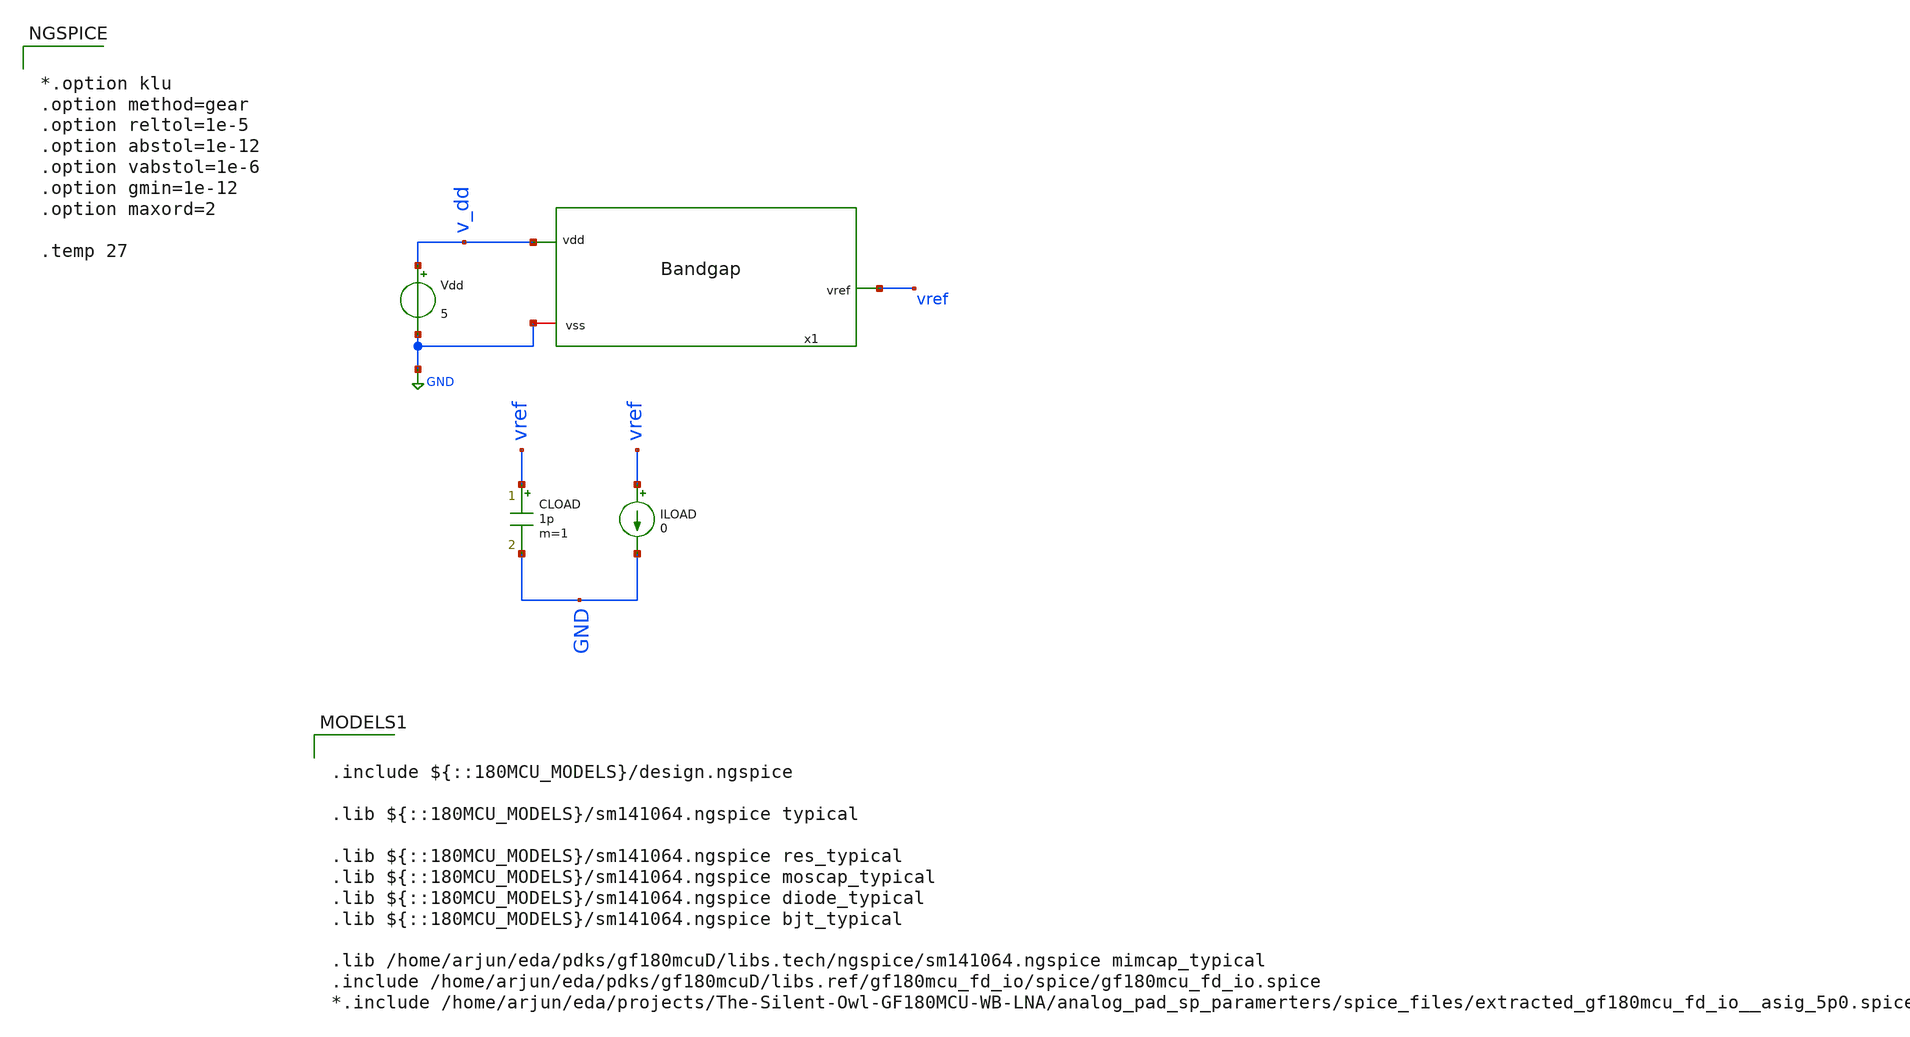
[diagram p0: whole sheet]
** sch_path: xschem/bandgap_tb.sch
**.subckt bandgap_tb
Vdd v_dd GND 5
CLOAD vref GND 1p m=1
ILOAD vref GND 0
x1 v_dd vref GND bandgap
**** begin user architecture code


*.option klu
.option method=gear
.option reltol=1e-5
.option abstol=1e-12
.option vabstol=1e-6
.option gmin=1e-12
.option maxord=2

.temp 27






.include ${::180MCU_MODELS}/design.ngspice

.lib ${::180MCU_MODELS}/sm141064.ngspice typical

.lib ${::180MCU_MODELS}/sm141064.ngspice res_typical
.lib ${::180MCU_MODELS}/sm141064.ngspice moscap_typical
.lib ${::180MCU_MODELS}/sm141064.ngspice diode_typical
.lib ${::180MCU_MODELS}/sm141064.ngspice bjt_typical

.lib /home/arjun/eda/pdks/gf180mcuD/libs.tech/ngspice/sm141064.ngspice mimcap_typical
.include /home/arjun/eda/pdks/gf180mcuD/libs.ref/gf180mcu_fd_io/spice/gf180mcu_fd_io.spice
*.include /home/arjun/eda/projects/The-Silent-Owl-GF180MCU-WB-LNA/analog_pad_sp_paramerters/spice_files/extracted_gf180mcu_fd_io__asig_5p0.spice




.control

* ============================================================
* GF180MCU Bandgap MOS OP Diagnostic
* Corrected version:
*   - No @m.$dev.m0[...] variable substitution
*   - Uses explicit hierarchical device paths
*
* Files:
*   bandgap_mos_op_detailed_report.txt
*   bandgap_mos_op_table.txt
* ============================================================

set noaskquit
set filetype=ascii
set numdgt=10
set wr_singlescale
set wr_vecnames

save all

echo GF180MCU_BANDGAP_ALL_MOS_OP_DETAILED_REPORT > bandgap_mos_op_detailed_report.txt
echo ============================================================ >>
+ bandgap_mos_op_detailed_report.txt
echo . >> bandgap_mos_op_detailed_report.txt

echo NOTE >> bandgap_mos_op_detailed_report.txt
echo ------------------------------------------------------------ >>
+ bandgap_mos_op_detailed_report.txt
echo This block uses explicit hierarchical OP paths. >> bandgap_mos_op_detailed_report.txt
echo Example path: @m.x1.xm8.m0[id]. >> bandgap_mos_op_detailed_report.txt
echo No device-name foreach substitution is used. >> bandgap_mos_op_detailed_report.txt
echo . >> bandgap_mos_op_detailed_report.txt

echo DEVICE VDD_V TEMP_C ID_A GM_S GMBS_S GDS_S VGS_V VDS_V VBS_V VTH_V VOV_ABS_V VDSAT_ABS_V
+ SAT_MARGIN_V GMID_1_PER_V RO_OHM GMRO > bandgap_mos_op_table.txt

foreach vddtest 3.0 4.5 5.0 5.5

  alter Vdd = $vddtest
  alter ILOAD = 0
  set temp = 27
  op

  let vdd_now = v(v_dd)
  let vref_now = v(vref)
  let idd_now = -i(vdd)
  let pdc_now = v(v_dd)*idd_now
  let pdc_now_uw = 1e6*pdc_now

  echo OP_SAMPLE VDD $vddtest TEMP_C 27 >> bandgap_mos_op_detailed_report.txt
  echo ============================================================ >>
+ bandgap_mos_op_detailed_report.txt

  echo TOP_LEVEL_VALUES >> bandgap_mos_op_detailed_report.txt
  echo VDD_V $&vdd_now >> bandgap_mos_op_detailed_report.txt
  echo VREF_V $&vref_now >> bandgap_mos_op_detailed_report.txt
  echo IDD_A $&idd_now >> bandgap_mos_op_detailed_report.txt
  echo PDC_W $&pdc_now >> bandgap_mos_op_detailed_report.txt
  echo PDC_uW $&pdc_now_uw >> bandgap_mos_op_detailed_report.txt
  echo . >> bandgap_mos_op_detailed_report.txt

  echo INTERNAL_NODE_VOLTAGES >> bandgap_mos_op_detailed_report.txt
  echo X1_VG1_V $&v(x1.vg1) >> bandgap_mos_op_detailed_report.txt
  echo X1_VG2_V $&v(x1.vg2) >> bandgap_mos_op_detailed_report.txt
  echo X1_VG3_V $&v(x1.vg3) >> bandgap_mos_op_detailed_report.txt
  echo X1_VG4_V $&v(x1.vg4) >> bandgap_mos_op_detailed_report.txt
  echo X1_NET1_V $&v(x1.net1) >> bandgap_mos_op_detailed_report.txt
  echo X1_NET2_V $&v(x1.net2) >> bandgap_mos_op_detailed_report.txt
  echo X1_NET3_V $&v(x1.net3) >> bandgap_mos_op_detailed_report.txt
  echo X1_NET4_V $&v(x1.net4) >> bandgap_mos_op_detailed_report.txt
  echo X1_NET5_V $&v(x1.net5) >> bandgap_mos_op_detailed_report.txt
  echo X1_NET6_V $&v(x1.net6) >> bandgap_mos_op_detailed_report.txt
  echo X1_NET7_V $&v(x1.net7) >> bandgap_mos_op_detailed_report.txt
  echo X1_NET8_V $&v(x1.net8) >> bandgap_mos_op_detailed_report.txt
  echo X1_NET9_V $&v(x1.net9) >> bandgap_mos_op_detailed_report.txt
  echo . >> bandgap_mos_op_detailed_report.txt

  * ============================================================
  * XM8
  * ============================================================

  let xm8_id = abs(@m.x1.xm8.m0[id])
  let xm8_gm = @m.x1.xm8.m0[gm]
  let xm8_gmbs = @m.x1.xm8.m0[gmbs]
  let xm8_gds = @m.x1.xm8.m0[gds]
  let xm8_vgs = @m.x1.xm8.m0[vgs]
  let xm8_vds = @m.x1.xm8.m0[vds]
  let xm8_vbs = @m.x1.xm8.m0[vbs]
  let xm8_vth = @m.x1.xm8.m0[vth]
  let xm8_vdsat = abs(@m.x1.xm8.m0[vdsat])
  let xm8_vov = abs(xm8_vgs)-abs(xm8_vth)
  let xm8_sat = abs(xm8_vds)-xm8_vdsat
  let xm8_gmid = xm8_gm/(xm8_id+1e-30)
  let xm8_ro = 1/(xm8_gds+1e-30)
  let xm8_gmro = xm8_gm*xm8_ro

  echo DEVICE XM8 >> bandgap_mos_op_detailed_report.txt
  echo ID_A $&xm8_id >> bandgap_mos_op_detailed_report.txt
  echo GM_S $&xm8_gm >> bandgap_mos_op_detailed_report.txt
  echo GMBS_S $&xm8_gmbs >> bandgap_mos_op_detailed_report.txt
  echo GDS_S $&xm8_gds >> bandgap_mos_op_detailed_report.txt
  echo VGS_V $&xm8_vgs >> bandgap_mos_op_detailed_report.txt
  echo VDS_V $&xm8_vds >> bandgap_mos_op_detailed_report.txt
  echo VBS_V $&xm8_vbs >> bandgap_mos_op_detailed_report.txt
  echo VTH_V $&xm8_vth >> bandgap_mos_op_detailed_report.txt
  echo VOV_ABS_V $&xm8_vov >> bandgap_mos_op_detailed_report.txt
  echo VDSAT_ABS_V $&xm8_vdsat >> bandgap_mos_op_detailed_report.txt
  echo SAT_MARGIN_V $&xm8_sat >> bandgap_mos_op_detailed_report.txt
  echo GMID_1_PER_V $&xm8_gmid >> bandgap_mos_op_detailed_report.txt
  echo RO_OHM $&xm8_ro >> bandgap_mos_op_detailed_report.txt
  echo GMRO $&xm8_gmro >> bandgap_mos_op_detailed_report.txt
  echo . >> bandgap_mos_op_detailed_report.txt
  echo XM8 $&vdd_now 27 $&xm8_id $&xm8_gm $&xm8_gmbs $&xm8_gds $&xm8_vgs $&xm8_vds $&xm8_vbs
+ $&xm8_vth $&xm8_vov $&xm8_vdsat $&xm8_sat $&xm8_gmid $&xm8_ro $&xm8_gmro >> bandgap_mos_op_table.txt

  * ============================================================
  * XM10
  * ============================================================

  let xm10_id = abs(@m.x1.xm10.m0[id])
  let xm10_gm = @m.x1.xm10.m0[gm]
  let xm10_gmbs = @m.x1.xm10.m0[gmbs]
  let xm10_gds = @m.x1.xm10.m0[gds]
  let xm10_vgs = @m.x1.xm10.m0[vgs]
  let xm10_vds = @m.x1.xm10.m0[vds]
  let xm10_vbs = @m.x1.xm10.m0[vbs]
  let xm10_vth = @m.x1.xm10.m0[vth]
  let xm10_vdsat = abs(@m.x1.xm10.m0[vdsat])
  let xm10_vov = abs(xm10_vgs)-abs(xm10_vth)
  let xm10_sat = abs(xm10_vds)-xm10_vdsat
  let xm10_gmid = xm10_gm/(xm10_id+1e-30)
  let xm10_ro = 1/(xm10_gds+1e-30)
  let xm10_gmro = xm10_gm*xm10_ro

  echo DEVICE XM10 >> bandgap_mos_op_detailed_report.txt
  echo ID_A $&xm10_id >> bandgap_mos_op_detailed_report.txt
  echo GM_S $&xm10_gm >> bandgap_mos_op_detailed_report.txt
  echo GMBS_S $&xm10_gmbs >> bandgap_mos_op_detailed_report.txt
  echo GDS_S $&xm10_gds >> bandgap_mos_op_detailed_report.txt
  echo VGS_V $&xm10_vgs >> bandgap_mos_op_detailed_report.txt
  echo VDS_V $&xm10_vds >> bandgap_mos_op_detailed_report.txt
  echo VBS_V $&xm10_vbs >> bandgap_mos_op_detailed_report.txt
  echo VTH_V $&xm10_vth >> bandgap_mos_op_detailed_report.txt
  echo VOV_ABS_V $&xm10_vov >> bandgap_mos_op_detailed_report.txt
  echo VDSAT_ABS_V $&xm10_vdsat >> bandgap_mos_op_detailed_report.txt
  echo SAT_MARGIN_V $&xm10_sat >> bandgap_mos_op_detailed_report.txt
  echo GMID_1_PER_V $&xm10_gmid >> bandgap_mos_op_detailed_report.txt
  echo RO_OHM $&xm10_ro >> bandgap_mos_op_detailed_report.txt
  echo GMRO $&xm10_gmro >> bandgap_mos_op_detailed_report.txt
  echo . >> bandgap_mos_op_detailed_report.txt
  echo XM10 $&vdd_now 27 $&xm10_id $&xm10_gm $&xm10_gmbs $&xm10_gds $&xm10_vgs $&xm10_vds $&xm10_vbs
+ $&xm10_vth $&xm10_vov $&xm10_vdsat $&xm10_sat $&xm10_gmid $&xm10_ro $&xm10_gmro >> bandgap_mos_op_table.txt

  * ============================================================
  * XM3
  * ============================================================

  let xm3_id = abs(@m.x1.xm3.m0[id])
  let xm3_gm = @m.x1.xm3.m0[gm]
  let xm3_gmbs = @m.x1.xm3.m0[gmbs]
  let xm3_gds = @m.x1.xm3.m0[gds]
  let xm3_vgs = @m.x1.xm3.m0[vgs]
  let xm3_vds = @m.x1.xm3.m0[vds]
  let xm3_vbs = @m.x1.xm3.m0[vbs]
  let xm3_vth = @m.x1.xm3.m0[vth]
  let xm3_vdsat = abs(@m.x1.xm3.m0[vdsat])
  let xm3_vov = abs(xm3_vgs)-abs(xm3_vth)
  let xm3_sat = abs(xm3_vds)-xm3_vdsat
  let xm3_gmid = xm3_gm/(xm3_id+1e-30)
  let xm3_ro = 1/(xm3_gds+1e-30)
  let xm3_gmro = xm3_gm*xm3_ro

  echo DEVICE XM3 >> bandgap_mos_op_detailed_report.txt
  echo ID_A $&xm3_id >> bandgap_mos_op_detailed_report.txt
  echo GM_S $&xm3_gm >> bandgap_mos_op_detailed_report.txt
  echo GMBS_S $&xm3_gmbs >> bandgap_mos_op_detailed_report.txt
  echo GDS_S $&xm3_gds >> bandgap_mos_op_detailed_report.txt
  echo VGS_V $&xm3_vgs >> bandgap_mos_op_detailed_report.txt
  echo VDS_V $&xm3_vds >> bandgap_mos_op_detailed_report.txt
  echo VBS_V $&xm3_vbs >> bandgap_mos_op_detailed_report.txt
  echo VTH_V $&xm3_vth >> bandgap_mos_op_detailed_report.txt
  echo VOV_ABS_V $&xm3_vov >> bandgap_mos_op_detailed_report.txt
  echo VDSAT_ABS_V $&xm3_vdsat >> bandgap_mos_op_detailed_report.txt
  echo SAT_MARGIN_V $&xm3_sat >> bandgap_mos_op_detailed_report.txt
  echo GMID_1_PER_V $&xm3_gmid >> bandgap_mos_op_detailed_report.txt
  echo RO_OHM $&xm3_ro >> bandgap_mos_op_detailed_report.txt
  echo GMRO $&xm3_gmro >> bandgap_mos_op_detailed_report.txt
  echo . >> bandgap_mos_op_detailed_report.txt
  echo XM3 $&vdd_now 27 $&xm3_id $&xm3_gm $&xm3_gmbs $&xm3_gds $&xm3_vgs $&xm3_vds $&xm3_vbs
+ $&xm3_vth $&xm3_vov $&xm3_vdsat $&xm3_sat $&xm3_gmid $&xm3_ro $&xm3_gmro >> bandgap_mos_op_table.txt

  * ============================================================
  * XM11
  * ============================================================

  let xm11_id = abs(@m.x1.xm11.m0[id])
  let xm11_gm = @m.x1.xm11.m0[gm]
  let xm11_gmbs = @m.x1.xm11.m0[gmbs]
  let xm11_gds = @m.x1.xm11.m0[gds]
  let xm11_vgs = @m.x1.xm11.m0[vgs]
  let xm11_vds = @m.x1.xm11.m0[vds]
  let xm11_vbs = @m.x1.xm11.m0[vbs]
  let xm11_vth = @m.x1.xm11.m0[vth]
  let xm11_vdsat = abs(@m.x1.xm11.m0[vdsat])
  let xm11_vov = abs(xm11_vgs)-abs(xm11_vth)
  let xm11_sat = abs(xm11_vds)-xm11_vdsat
  let xm11_gmid = xm11_gm/(xm11_id+1e-30)
  let xm11_ro = 1/(xm11_gds+1e-30)
  let xm11_gmro = xm11_gm*xm11_ro

  echo DEVICE XM11 >> bandgap_mos_op_detailed_report.txt
  echo ID_A $&xm11_id >> bandgap_mos_op_detailed_report.txt
  echo GM_S $&xm11_gm >> bandgap_mos_op_detailed_report.txt
  echo GMBS_S $&xm11_gmbs >> bandgap_mos_op_detailed_report.txt
  echo GDS_S $&xm11_gds >> bandgap_mos_op_detailed_report.txt
  echo VGS_V $&xm11_vgs >> bandgap_mos_op_detailed_report.txt
  echo VDS_V $&xm11_vds >> bandgap_mos_op_detailed_report.txt
  echo VBS_V $&xm11_vbs >> bandgap_mos_op_detailed_report.txt
  echo VTH_V $&xm11_vth >> bandgap_mos_op_detailed_report.txt
  echo VOV_ABS_V $&xm11_vov >> bandgap_mos_op_detailed_report.txt
  echo VDSAT_ABS_V $&xm11_vdsat >> bandgap_mos_op_detailed_report.txt
  echo SAT_MARGIN_V $&xm11_sat >> bandgap_mos_op_detailed_report.txt
  echo GMID_1_PER_V $&xm11_gmid >> bandgap_mos_op_detailed_report.txt
  echo RO_OHM $&xm11_ro >> bandgap_mos_op_detailed_report.txt
  echo GMRO $&xm11_gmro >> bandgap_mos_op_detailed_report.txt
  echo . >> bandgap_mos_op_detailed_report.txt
  echo XM11 $&vdd_now 27 $&xm11_id $&xm11_gm $&xm11_gmbs $&xm11_gds $&xm11_vgs $&xm11_vds $&xm11_vbs
+ $&xm11_vth $&xm11_vov $&xm11_vdsat $&xm11_sat $&xm11_gmid $&xm11_ro $&xm11_gmro >> bandgap_mos_op_table.txt

  * ============================================================
  * XM12
  * ============================================================

  let xm12_id = abs(@m.x1.xm12.m0[id])
  let xm12_gm = @m.x1.xm12.m0[gm]
  let xm12_gmbs = @m.x1.xm12.m0[gmbs]
  let xm12_gds = @m.x1.xm12.m0[gds]
  let xm12_vgs = @m.x1.xm12.m0[vgs]
  let xm12_vds = @m.x1.xm12.m0[vds]
  let xm12_vbs = @m.x1.xm12.m0[vbs]
  let xm12_vth = @m.x1.xm12.m0[vth]
  let xm12_vdsat = abs(@m.x1.xm12.m0[vdsat])
  let xm12_vov = abs(xm12_vgs)-abs(xm12_vth)
  let xm12_sat = abs(xm12_vds)-xm12_vdsat
  let xm12_gmid = xm12_gm/(xm12_id+1e-30)
  let xm12_ro = 1/(xm12_gds+1e-30)
  let xm12_gmro = xm12_gm*xm12_ro

  echo DEVICE XM12 >> bandgap_mos_op_detailed_report.txt
  echo ID_A $&xm12_id >> bandgap_mos_op_detailed_report.txt
  echo GM_S $&xm12_gm >> bandgap_mos_op_detailed_report.txt
  echo GMBS_S $&xm12_gmbs >> bandgap_mos_op_detailed_report.txt
  echo GDS_S $&xm12_gds >> bandgap_mos_op_detailed_report.txt
  echo VGS_V $&xm12_vgs >> bandgap_mos_op_detailed_report.txt
  echo VDS_V $&xm12_vds >> bandgap_mos_op_detailed_report.txt
  echo VBS_V $&xm12_vbs >> bandgap_mos_op_detailed_report.txt
  echo VTH_V $&xm12_vth >> bandgap_mos_op_detailed_report.txt
  echo VOV_ABS_V $&xm12_vov >> bandgap_mos_op_detailed_report.txt
  echo VDSAT_ABS_V $&xm12_vdsat >> bandgap_mos_op_detailed_report.txt
  echo SAT_MARGIN_V $&xm12_sat >> bandgap_mos_op_detailed_report.txt
  echo GMID_1_PER_V $&xm12_gmid >> bandgap_mos_op_detailed_report.txt
  echo RO_OHM $&xm12_ro >> bandgap_mos_op_detailed_report.txt
  echo GMRO $&xm12_gmro >> bandgap_mos_op_detailed_report.txt
  echo . >> bandgap_mos_op_detailed_report.txt
  echo XM12 $&vdd_now 27 $&xm12_id $&xm12_gm $&xm12_gmbs $&xm12_gds $&xm12_vgs $&xm12_vds $&xm12_vbs
+ $&xm12_vth $&xm12_vov $&xm12_vdsat $&xm12_sat $&xm12_gmid $&xm12_ro $&xm12_gmro >> bandgap_mos_op_table.txt

  * ============================================================
  * XM14
  * ============================================================

  let xm14_id = abs(@m.x1.xm14.m0[id])
  let xm14_gm = @m.x1.xm14.m0[gm]
  let xm14_gmbs = @m.x1.xm14.m0[gmbs]
  let xm14_gds = @m.x1.xm14.m0[gds]
  let xm14_vgs = @m.x1.xm14.m0[vgs]
  let xm14_vds = @m.x1.xm14.m0[vds]
  let xm14_vbs = @m.x1.xm14.m0[vbs]
  let xm14_vth = @m.x1.xm14.m0[vth]
  let xm14_vdsat = abs(@m.x1.xm14.m0[vdsat])
  let xm14_vov = abs(xm14_vgs)-abs(xm14_vth)
  let xm14_sat = abs(xm14_vds)-xm14_vdsat
  let xm14_gmid = xm14_gm/(xm14_id+1e-30)
  let xm14_ro = 1/(xm14_gds+1e-30)
  let xm14_gmro = xm14_gm*xm14_ro

  echo DEVICE XM14 >> bandgap_mos_op_detailed_report.txt
  echo ID_A $&xm14_id >> bandgap_mos_op_detailed_report.txt
  echo GM_S $&xm14_gm >> bandgap_mos_op_detailed_report.txt
  echo GMBS_S $&xm14_gmbs >> bandgap_mos_op_detailed_report.txt
  echo GDS_S $&xm14_gds >> bandgap_mos_op_detailed_report.txt
  echo VGS_V $&xm14_vgs >> bandgap_mos_op_detailed_report.txt
  echo VDS_V $&xm14_vds >> bandgap_mos_op_detailed_report.txt
  echo VBS_V $&xm14_vbs >> bandgap_mos_op_detailed_report.txt
  echo VTH_V $&xm14_vth >> bandgap_mos_op_detailed_report.txt
  echo VOV_ABS_V $&xm14_vov >> bandgap_mos_op_detailed_report.txt
  echo VDSAT_ABS_V $&xm14_vdsat >> bandgap_mos_op_detailed_report.txt
  echo SAT_MARGIN_V $&xm14_sat >> bandgap_mos_op_detailed_report.txt
  echo GMID_1_PER_V $&xm14_gmid >> bandgap_mos_op_detailed_report.txt
  echo RO_OHM $&xm14_ro >> bandgap_mos_op_detailed_report.txt
  echo GMRO $&xm14_gmro >> bandgap_mos_op_detailed_report.txt
  echo . >> bandgap_mos_op_detailed_report.txt
  echo XM14 $&vdd_now 27 $&xm14_id $&xm14_gm $&xm14_gmbs $&xm14_gds $&xm14_vgs $&xm14_vds $&xm14_vbs
+ $&xm14_vth $&xm14_vov $&xm14_vdsat $&xm14_sat $&xm14_gmid $&xm14_ro $&xm14_gmro >> bandgap_mos_op_table.txt

  * ============================================================
  * XM5
  * ============================================================

  let xm5_id = abs(@m.x1.xm5.m0[id])
  let xm5_gm = @m.x1.xm5.m0[gm]
  let xm5_gmbs = @m.x1.xm5.m0[gmbs]
  let xm5_gds = @m.x1.xm5.m0[gds]
  let xm5_vgs = @m.x1.xm5.m0[vgs]
  let xm5_vds = @m.x1.xm5.m0[vds]
  let xm5_vbs = @m.x1.xm5.m0[vbs]
  let xm5_vth = @m.x1.xm5.m0[vth]
  let xm5_vdsat = abs(@m.x1.xm5.m0[vdsat])
  let xm5_vov = abs(xm5_vgs)-abs(xm5_vth)
  let xm5_sat = abs(xm5_vds)-xm5_vdsat
  let xm5_gmid = xm5_gm/(xm5_id+1e-30)
  let xm5_ro = 1/(xm5_gds+1e-30)
  let xm5_gmro = xm5_gm*xm5_ro

  echo DEVICE XM5 >> bandgap_mos_op_detailed_report.txt
  echo ID_A $&xm5_id >> bandgap_mos_op_detailed_report.txt
  echo GM_S $&xm5_gm >> bandgap_mos_op_detailed_report.txt
  echo GMBS_S $&xm5_gmbs >> bandgap_mos_op_detailed_report.txt
  echo GDS_S $&xm5_gds >> bandgap_mos_op_detailed_report.txt
  echo VGS_V $&xm5_vgs >> bandgap_mos_op_detailed_report.txt
  echo VDS_V $&xm5_vds >> bandgap_mos_op_detailed_report.txt
  echo VBS_V $&xm5_vbs >> bandgap_mos_op_detailed_report.txt
  echo VTH_V $&xm5_vth >> bandgap_mos_op_detailed_report.txt
  echo VOV_ABS_V $&xm5_vov >> bandgap_mos_op_detailed_report.txt
  echo VDSAT_ABS_V $&xm5_vdsat >> bandgap_mos_op_detailed_report.txt
  echo SAT_MARGIN_V $&xm5_sat >> bandgap_mos_op_detailed_report.txt
  echo GMID_1_PER_V $&xm5_gmid >> bandgap_mos_op_detailed_report.txt
  echo RO_OHM $&xm5_ro >> bandgap_mos_op_detailed_report.txt
  echo GMRO $&xm5_gmro >> bandgap_mos_op_detailed_report.txt
  echo . >> bandgap_mos_op_detailed_report.txt
  echo XM5 $&vdd_now 27 $&xm5_id $&xm5_gm $&xm5_gmbs $&xm5_gds $&xm5_vgs $&xm5_vds $&xm5_vbs
+ $&xm5_vth $&xm5_vov $&xm5_vdsat $&xm5_sat $&xm5_gmid $&xm5_ro $&xm5_gmro >> bandgap_mos_op_table.txt

  * ============================================================
  * XM6
  * ============================================================

  let xm6_id = abs(@m.x1.xm6.m0[id])
  let xm6_gm = @m.x1.xm6.m0[gm]
  let xm6_gmbs = @m.x1.xm6.m0[gmbs]
  let xm6_gds = @m.x1.xm6.m0[gds]
  let xm6_vgs = @m.x1.xm6.m0[vgs]
  let xm6_vds = @m.x1.xm6.m0[vds]
  let xm6_vbs = @m.x1.xm6.m0[vbs]
  let xm6_vth = @m.x1.xm6.m0[vth]
  let xm6_vdsat = abs(@m.x1.xm6.m0[vdsat])
  let xm6_vov = abs(xm6_vgs)-abs(xm6_vth)
  let xm6_sat = abs(xm6_vds)-xm6_vdsat
  let xm6_gmid = xm6_gm/(xm6_id+1e-30)
  let xm6_ro = 1/(xm6_gds+1e-30)
  let xm6_gmro = xm6_gm*xm6_ro

  echo DEVICE XM6 >> bandgap_mos_op_detailed_report.txt
  echo ID_A $&xm6_id >> bandgap_mos_op_detailed_report.txt
  echo GM_S $&xm6_gm >> bandgap_mos_op_detailed_report.txt
  echo GMBS_S $&xm6_gmbs >> bandgap_mos_op_detailed_report.txt
  echo GDS_S $&xm6_gds >> bandgap_mos_op_detailed_report.txt
  echo VGS_V $&xm6_vgs >> bandgap_mos_op_detailed_report.txt
  echo VDS_V $&xm6_vds >> bandgap_mos_op_detailed_report.txt
  echo VBS_V $&xm6_vbs >> bandgap_mos_op_detailed_report.txt
  echo VTH_V $&xm6_vth >> bandgap_mos_op_detailed_report.txt
  echo VOV_ABS_V $&xm6_vov >> bandgap_mos_op_detailed_report.txt
  echo VDSAT_ABS_V $&xm6_vdsat >> bandgap_mos_op_detailed_report.txt
  echo SAT_MARGIN_V $&xm6_sat >> bandgap_mos_op_detailed_report.txt
  echo GMID_1_PER_V $&xm6_gmid >> bandgap_mos_op_detailed_report.txt
  echo RO_OHM $&xm6_ro >> bandgap_mos_op_detailed_report.txt
  echo GMRO $&xm6_gmro >> bandgap_mos_op_detailed_report.txt
  echo . >> bandgap_mos_op_detailed_report.txt
  echo XM6 $&vdd_now 27 $&xm6_id $&xm6_gm $&xm6_gmbs $&xm6_gds $&xm6_vgs $&xm6_vds $&xm6_vbs
+ $&xm6_vth $&xm6_vov $&xm6_vdsat $&xm6_sat $&xm6_gmid $&xm6_ro $&xm6_gmro >> bandgap_mos_op_table.txt

  * ============================================================
  * XM7
  * ============================================================

  let xm7_id = abs(@m.x1.xm7.m0[id])
  let xm7_gm = @m.x1.xm7.m0[gm]
  let xm7_gmbs = @m.x1.xm7.m0[gmbs]
  let xm7_gds = @m.x1.xm7.m0[gds]
  let xm7_vgs = @m.x1.xm7.m0[vgs]
  let xm7_vds = @m.x1.xm7.m0[vds]
  let xm7_vbs = @m.x1.xm7.m0[vbs]
  let xm7_vth = @m.x1.xm7.m0[vth]
  let xm7_vdsat = abs(@m.x1.xm7.m0[vdsat])
  let xm7_vov = abs(xm7_vgs)-abs(xm7_vth)
  let xm7_sat = abs(xm7_vds)-xm7_vdsat
  let xm7_gmid = xm7_gm/(xm7_id+1e-30)
  let xm7_ro = 1/(xm7_gds+1e-30)
  let xm7_gmro = xm7_gm*xm7_ro

  echo DEVICE XM7 >> bandgap_mos_op_detailed_report.txt
  echo ID_A $&xm7_id >> bandgap_mos_op_detailed_report.txt
  echo GM_S $&xm7_gm >> bandgap_mos_op_detailed_report.txt
  echo GMBS_S $&xm7_gmbs >> bandgap_mos_op_detailed_report.txt
  echo GDS_S $&xm7_gds >> bandgap_mos_op_detailed_report.txt
  echo VGS_V $&xm7_vgs >> bandgap_mos_op_detailed_report.txt
  echo VDS_V $&xm7_vds >> bandgap_mos_op_detailed_report.txt
  echo VBS_V $&xm7_vbs >> bandgap_mos_op_detailed_report.txt
  echo VTH_V $&xm7_vth >> bandgap_mos_op_detailed_report.txt
  echo VOV_ABS_V $&xm7_vov >> bandgap_mos_op_detailed_report.txt
  echo VDSAT_ABS_V $&xm7_vdsat >> bandgap_mos_op_detailed_report.txt
  echo SAT_MARGIN_V $&xm7_sat >> bandgap_mos_op_detailed_report.txt
  echo GMID_1_PER_V $&xm7_gmid >> bandgap_mos_op_detailed_report.txt
  echo RO_OHM $&xm7_ro >> bandgap_mos_op_detailed_report.txt
  echo GMRO $&xm7_gmro >> bandgap_mos_op_detailed_report.txt
  echo . >> bandgap_mos_op_detailed_report.txt
  echo XM7 $&vdd_now 27 $&xm7_id $&xm7_gm $&xm7_gmbs $&xm7_gds $&xm7_vgs $&xm7_vds $&xm7_vbs
+ $&xm7_vth $&xm7_vov $&xm7_vdsat $&xm7_sat $&xm7_gmid $&xm7_ro $&xm7_gmro >> bandgap_mos_op_table.txt

  * ============================================================
  * XM9
  * ============================================================

  let xm9_id = abs(@m.x1.xm9.m0[id])
  let xm9_gm = @m.x1.xm9.m0[gm]
  let xm9_gmbs = @m.x1.xm9.m0[gmbs]
  let xm9_gds = @m.x1.xm9.m0[gds]
  let xm9_vgs = @m.x1.xm9.m0[vgs]
  let xm9_vds = @m.x1.xm9.m0[vds]
  let xm9_vbs = @m.x1.xm9.m0[vbs]
  let xm9_vth = @m.x1.xm9.m0[vth]
  let xm9_vdsat = abs(@m.x1.xm9.m0[vdsat])
  let xm9_vov = abs(xm9_vgs)-abs(xm9_vth)
  let xm9_sat = abs(xm9_vds)-xm9_vdsat
  let xm9_gmid = xm9_gm/(xm9_id+1e-30)
  let xm9_ro = 1/(xm9_gds+1e-30)
  let xm9_gmro = xm9_gm*xm9_ro

  echo DEVICE XM9 >> bandgap_mos_op_detailed_report.txt
  echo ID_A $&xm9_id >> bandgap_mos_op_detailed_report.txt
  echo GM_S $&xm9_gm >> bandgap_mos_op_detailed_report.txt
  echo GMBS_S $&xm9_gmbs >> bandgap_mos_op_detailed_report.txt
  echo GDS_S $&xm9_gds >> bandgap_mos_op_detailed_report.txt
  echo VGS_V $&xm9_vgs >> bandgap_mos_op_detailed_report.txt
  echo VDS_V $&xm9_vds >> bandgap_mos_op_detailed_report.txt
  echo VBS_V $&xm9_vbs >> bandgap_mos_op_detailed_report.txt
  echo VTH_V $&xm9_vth >> bandgap_mos_op_detailed_report.txt
  echo VOV_ABS_V $&xm9_vov >> bandgap_mos_op_detailed_report.txt
  echo VDSAT_ABS_V $&xm9_vdsat >> bandgap_mos_op_detailed_report.txt
  echo SAT_MARGIN_V $&xm9_sat >> bandgap_mos_op_detailed_report.txt
  echo GMID_1_PER_V $&xm9_gmid >> bandgap_mos_op_detailed_report.txt
  echo RO_OHM $&xm9_ro >> bandgap_mos_op_detailed_report.txt
  echo GMRO $&xm9_gmro >> bandgap_mos_op_detailed_report.txt
  echo . >> bandgap_mos_op_detailed_report.txt
  echo XM9 $&vdd_now 27 $&xm9_id $&xm9_gm $&xm9_gmbs $&xm9_gds $&xm9_vgs $&xm9_vds $&xm9_vbs
+ $&xm9_vth $&xm9_vov $&xm9_vdsat $&xm9_sat $&xm9_gmid $&xm9_ro $&xm9_gmro >> bandgap_mos_op_table.txt

  * ============================================================
  * XM13
  * ============================================================

  let xm13_id = abs(@m.x1.xm13.m0[id])
  let xm13_gm = @m.x1.xm13.m0[gm]
  let xm13_gmbs = @m.x1.xm13.m0[gmbs]
  let xm13_gds = @m.x1.xm13.m0[gds]
  let xm13_vgs = @m.x1.xm13.m0[vgs]
  let xm13_vds = @m.x1.xm13.m0[vds]
  let xm13_vbs = @m.x1.xm13.m0[vbs]
  let xm13_vth = @m.x1.xm13.m0[vth]
  let xm13_vdsat = abs(@m.x1.xm13.m0[vdsat])
  let xm13_vov = abs(xm13_vgs)-abs(xm13_vth)
  let xm13_sat = abs(xm13_vds)-xm13_vdsat
  let xm13_gmid = xm13_gm/(xm13_id+1e-30)
  let xm13_ro = 1/(xm13_gds+1e-30)
  let xm13_gmro = xm13_gm*xm13_ro

  echo DEVICE XM13 >> bandgap_mos_op_detailed_report.txt
  echo ID_A $&xm13_id >> bandgap_mos_op_detailed_report.txt
  echo GM_S $&xm13_gm >> bandgap_mos_op_detailed_report.txt
  echo GMBS_S $&xm13_gmbs >> bandgap_mos_op_detailed_report.txt
  echo GDS_S $&xm13_gds >> bandgap_mos_op_detailed_report.txt
  echo VGS_V $&xm13_vgs >> bandgap_mos_op_detailed_report.txt
  echo VDS_V $&xm13_vds >> bandgap_mos_op_detailed_report.txt
  echo VBS_V $&xm13_vbs >> bandgap_mos_op_detailed_report.txt
  echo VTH_V $&xm13_vth >> bandgap_mos_op_detailed_report.txt
  echo VOV_ABS_V $&xm13_vov >> bandgap_mos_op_detailed_report.txt
  echo VDSAT_ABS_V $&xm13_vdsat >> bandgap_mos_op_detailed_report.txt
  echo SAT_MARGIN_V $&xm13_sat >> bandgap_mos_op_detailed_report.txt
  echo GMID_1_PER_V $&xm13_gmid >> bandgap_mos_op_detailed_report.txt
  echo RO_OHM $&xm13_ro >> bandgap_mos_op_detailed_report.txt
  echo GMRO $&xm13_gmro >> bandgap_mos_op_detailed_report.txt
  echo . >> bandgap_mos_op_detailed_report.txt
  echo XM13 $&vdd_now 27 $&xm13_id $&xm13_gm $&xm13_gmbs $&xm13_gds $&xm13_vgs $&xm13_vds $&xm13_vbs
+ $&xm13_vth $&xm13_vov $&xm13_vdsat $&xm13_sat $&xm13_gmid $&xm13_ro $&xm13_gmro >> bandgap_mos_op_table.txt

  echo END_OP_SAMPLE VDD $vddtest >> bandgap_mos_op_detailed_report.txt
  echo . >> bandgap_mos_op_detailed_report.txt

end

echo INTERPRETATION_GUIDE >> bandgap_mos_op_detailed_report.txt
echo ------------------------------------------------------------ >>
+ bandgap_mos_op_detailed_report.txt
echo SAT_MARGIN_V = abs(VDS)-abs(VDSAT). Positive means saturation by first-order check. >>
+ bandgap_mos_op_detailed_report.txt
echo GMID_1_PER_V = gm divided by absolute drain current. >> bandgap_mos_op_detailed_report.txt
echo RO_OHM = 1/gds. Larger ro improves current-source behavior and line regulation. >>
+ bandgap_mos_op_detailed_report.txt
echo GMRO = gm/gds. Larger gmro means higher intrinsic gain. >> bandgap_mos_op_detailed_report.txt
echo Inspect devices with low SAT_MARGIN_V, low RO_OHM, or low GMRO. >>
+ bandgap_mos_op_detailed_report.txt
echo . >> bandgap_mos_op_detailed_report.txt

echo FILES_WRITTEN >> bandgap_mos_op_detailed_report.txt
echo ------------------------------------------------------------ >>
+ bandgap_mos_op_detailed_report.txt
echo bandgap_mos_op_detailed_report.txt >> bandgap_mos_op_detailed_report.txt
echo bandgap_mos_op_table.txt >> bandgap_mos_op_detailed_report.txt
echo . >> bandgap_mos_op_detailed_report.txt

echo ============================================================ >>
+ bandgap_mos_op_detailed_report.txt
echo END_OF_ALL_MOS_OP_REPORT >> bandgap_mos_op_detailed_report.txt
echo ============================================================ >>
+ bandgap_mos_op_detailed_report.txt

.endc



**** end user architecture code
**.ends

* expanding   symbol:  /home/arjun/eda/projects/The-Silent-Owl-GF180MCU-WB-LNA/xschem/bandgap.sym #
*+ of pins=3
** sym_path: xschem/bandgap.sym
** sch_path: xschem/bandgap.sch
.subckt bandgap vdd vref vss
*.ipin vdd
*.iopin vss
*.opin vref
XQ1 vss vss net4 pnp_05p00x05p00 m=40 par=40
XQ2 vss vss net6 pnp_05p00x05p00 m=40 par=40
XQ3 vss vss net9 pnp_05p00x05p00 m=2 par=2
XM12 net2 vg4 vdd vdd pfet_05v0 L=1u W=50u nf=10 ad='int((nf+1)/2) * W/nf * 0.18u' as='int((nf+2)/2) * W/nf * 0.18u'
+ pd='2*int((nf+1)/2) * (W/nf + 0.18u)' ps='2*int((nf+2)/2) * (W/nf + 0.18u)' nrd='0.18u / W' nrs='0.18u / W'
+ sa=0 sb=0 sd=0 m=1
XM13 vg3 vg2 net5 vss nfet_05v0 L=1u W=15u nf=3 ad='int((nf+1)/2) * W/nf * 0.18u' as='int((nf+2)/2) * W/nf * 0.18u'
+ pd='2*int((nf+1)/2) * (W/nf + 0.18u)' ps='2*int((nf+2)/2) * (W/nf + 0.18u)' nrd='0.18u / W' nrs='0.18u / W'
+ sa=0 sb=0 sd=0 m=1
XM14 net1 vg4 vdd vdd pfet_05v0 L=1u W=50u nf=10 ad='int((nf+1)/2) * W/nf * 0.18u' as='int((nf+2)/2) * W/nf * 0.18u'
+ pd='2*int((nf+1)/2) * (W/nf + 0.18u)' ps='2*int((nf+2)/2) * (W/nf + 0.18u)' nrd='0.18u / W' nrs='0.18u / W'
+ sa=0 sb=0 sd=0 m=1
XM1 vg2 vg3 net1 vdd pfet_05v0 L=1u W=50u nf=10 ad='int((nf+1)/2) * W/nf * 0.18u' as='int((nf+2)/2) * W/nf * 0.18u'
+ pd='2*int((nf+1)/2) * (W/nf + 0.18u)' ps='2*int((nf+2)/2) * (W/nf + 0.18u)' nrd='0.18u / W' nrs='0.18u / W'
+ sa=0 sb=0 sd=0 m=1
XM2 vg4 vg3 net2 vdd pfet_05v0 L=1u W=50u nf=10 ad='int((nf+1)/2) * W/nf * 0.18u' as='int((nf+2)/2) * W/nf * 0.18u'
+ pd='2*int((nf+1)/2) * (W/nf + 0.18u)' ps='2*int((nf+2)/2) * (W/nf + 0.18u)' nrd='0.18u / W' nrs='0.18u / W'
+ sa=0 sb=0 sd=0 m=1
XM3 net3 vg4 vdd vdd pfet_05v0 L=1u W=50u nf=10 ad='int((nf+1)/2) * W/nf * 0.18u' as='int((nf+2)/2) * W/nf * 0.18u'
+ pd='2*int((nf+1)/2) * (W/nf + 0.18u)' ps='2*int((nf+2)/2) * (W/nf + 0.18u)' nrd='0.18u / W' nrs='0.18u / W'
+ sa=0 sb=0 sd=0 m=1
XM4 vref vg3 net3 vdd pfet_05v0 L=1u W=50u nf=10 ad='int((nf+1)/2) * W/nf * 0.18u' as='int((nf+2)/2) * W/nf * 0.18u'
+ pd='2*int((nf+1)/2) * (W/nf + 0.18u)' ps='2*int((nf+2)/2) * (W/nf + 0.18u)' nrd='0.18u / W' nrs='0.18u / W'
+ sa=0 sb=0 sd=0 m=1
XM5 vg2 vg2 vg3 vdd pfet_05v0 L=10u W=0.5u nf=1 ad='int((nf+1)/2) * W/nf * 0.18u' as='int((nf+2)/2) * W/nf * 0.18u'
+ pd='2*int((nf+1)/2) * (W/nf + 0.18u)' ps='2*int((nf+2)/2) * (W/nf + 0.18u)' nrd='0.18u / W' nrs='0.18u / W'
+ sa=0 sb=0 sd=0 m=1
XM6 vg1 vg2 net8 vss nfet_05v0 L=1u W=15u nf=3 ad='int((nf+1)/2) * W/nf * 0.18u' as='int((nf+2)/2) * W/nf * 0.18u'
+ pd='2*int((nf+1)/2) * (W/nf + 0.18u)' ps='2*int((nf+2)/2) * (W/nf + 0.18u)' nrd='0.18u / W' nrs='0.18u / W'
+ sa=0 sb=0 sd=0 m=1
XM9 net8 vg1 net9 vss nfet_05v0 L=1u W=15u nf=3 ad='int((nf+1)/2) * W/nf * 0.18u' as='int((nf+2)/2) * W/nf * 0.18u'
+ pd='2*int((nf+1)/2) * (W/nf + 0.18u)' ps='2*int((nf+2)/2) * (W/nf + 0.18u)' nrd='0.18u / W' nrs='0.18u / W'
+ sa=0 sb=0 sd=0 m=1
XM7 net5 vg1 net7 vss nfet_05v0 L=1u W=15u nf=3 ad='int((nf+1)/2) * W/nf * 0.18u' as='int((nf+2)/2) * W/nf * 0.18u'
+ pd='2*int((nf+1)/2) * (W/nf + 0.18u)' ps='2*int((nf+2)/2) * (W/nf + 0.18u)' nrd='0.18u / W' nrs='0.18u / W'
+ sa=0 sb=0 sd=0 m=1
XR6 net6 net7 vss ppolyf_u_1k_6p0 r_width=3u r_length=18u m=1
XR7 net4 vref vss ppolyf_u_1k_6p0 r_width=3u r_length=116.2u m=1
XR8 vg1 vg2 vss ppolyf_u_1k_6p0 r_width=3u r_length=30u m=1
XR5 vg3 vg4 vss ppolyf_u_1k_6p0 r_width=3u r_length=30u m=1
.ends

.GLOBAL GND
.end
